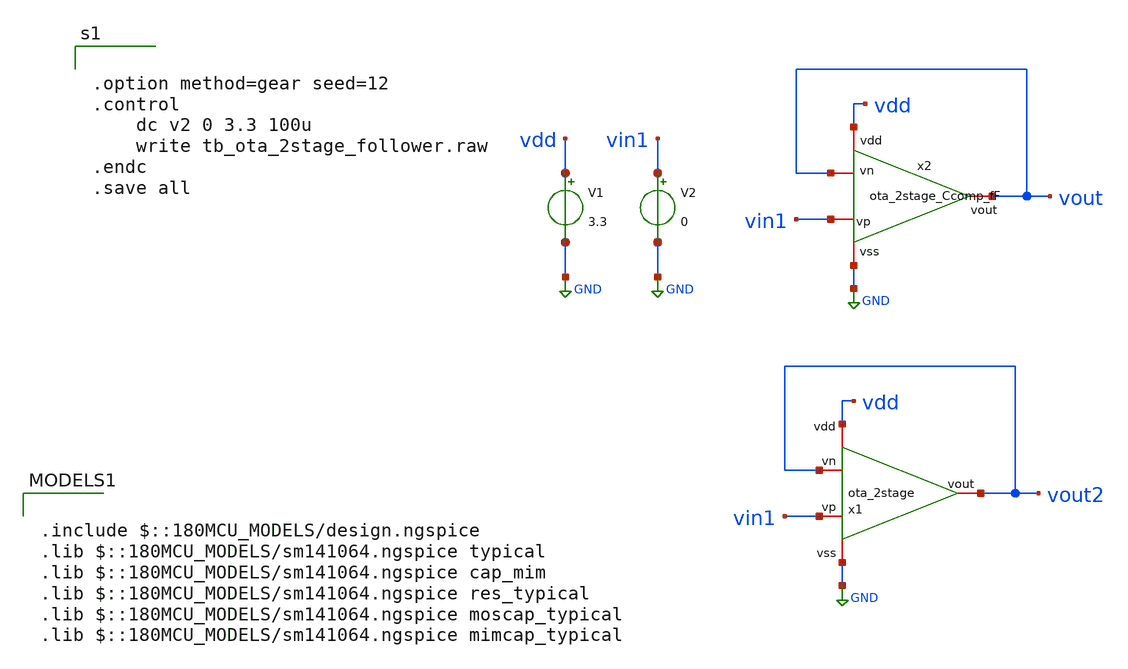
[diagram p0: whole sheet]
** sch_path: designs/libs/core_LIF_comp/tb_ota_2stage/tb_ota_2stage_follower.sch
**.subckt tb_ota_2stage_follower
x2 vdd GND vin1 vout vout ota_2stage_Ccomp_fF
V1 vdd GND 3.3
V2 vin1 GND 0
x1 vdd vout2 vout2 vin1 GND ota_2stage
**** begin user architecture code


.option method=gear seed=12
.control
    dc v2 0 3.3 100u
    write tb_ota_2stage_follower.raw
.endc
.save all



.include $::180MCU_MODELS/design.ngspice
.lib $::180MCU_MODELS/sm141064.ngspice typical
.lib $::180MCU_MODELS/sm141064.ngspice cap_mim
.lib $::180MCU_MODELS/sm141064.ngspice res_typical
.lib $::180MCU_MODELS/sm141064.ngspice moscap_typical
.lib $::180MCU_MODELS/sm141064.ngspice mimcap_typical

**** end user architecture code
**.ends
.GLOBAL GND
.end
